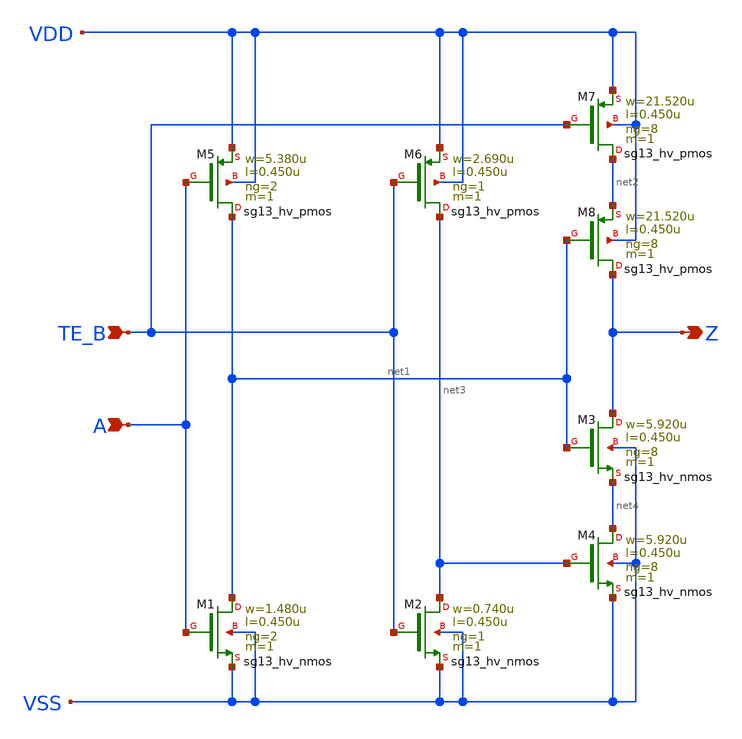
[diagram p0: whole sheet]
** sch_path: ihp-sg13g2/libs.ref/sg13g2_stdcell_hv/sch/xschem/sg13g2_hv_ebufn_8.sch
* Copyright 2023 IHP PDK Authors
* Licensed under the Apache License, Version 2.0 (the "License");
* you may not use this file except in compliance with the License.
* You may obtain a copy of the License at
* https://www.apache.org/licenses/LICENSE-2.0
* Unless required by applicable law or agreed to in writing, software
* distributed under the License is distributed on an "AS IS" BASIS,
* WITHOUT WARRANTIES OR CONDITIONS OF ANY KIND, either express or implied.
* See the License for the specific language governing permissions and
* limitations under the License.
**.subckt sg13g2_hv_ebufn_8 A TE_B Z
*.ipin A
*.ipin TE_B
*.opin Z
XM1 net1 A VSS VSS sg13_hv_nmos w=1.480u l=0.450u ng=2 m=1 mm_ok=1
XM2 net3 TE_B VSS VSS sg13_hv_nmos w=0.740u l=0.450u ng=1 m=1 mm_ok=1
XM3 Z net1 net4 VSS sg13_hv_nmos w=5.920u l=0.450u ng=8 m=1 mm_ok=1
XM4 net4 net3 VSS VSS sg13_hv_nmos w=5.920u l=0.450u ng=8 m=1 mm_ok=1
XM5 net1 A VDD VDD sg13_hv_pmos w=5.380u l=0.450u ng=2 m=1 mm_ok=1
XM6 net3 TE_B VDD VDD sg13_hv_pmos w=2.690u l=0.450u ng=1 m=1 mm_ok=1
XM7 net2 TE_B VDD VDD sg13_hv_pmos w=21.520u l=0.450u ng=8 m=1 mm_ok=1
XM8 Z net1 net2 VDD sg13_hv_pmos w=21.520u l=0.450u ng=8 m=1 mm_ok=1
**.ends
.end
